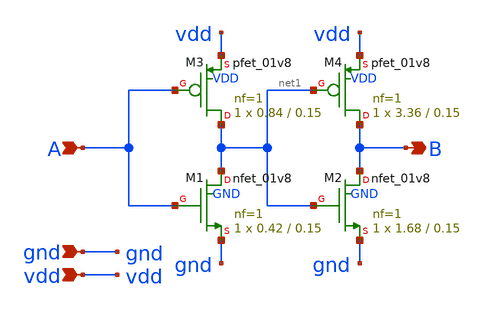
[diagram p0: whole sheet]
** sch_path: xschem/buffer_fo4.sch
**.subckt buffer_fo4 A B vdd gnd
*.ipin A
*.opin B
*.ipin vdd
*.ipin gnd
XM1 net1 A gnd GND sky130_fd_pr__nfet_01v8 L=0.15 W=0.42 nf=1 ad='int((nf+1)/2) * W/nf * 0.29' as='int((nf+2)/2) * W/nf * 0.29'
+ pd='2*int((nf+1)/2) * (W/nf + 0.29)' ps='2*int((nf+2)/2) * (W/nf + 0.29)' nrd='0.29 / W' nrs='0.29 / W'
+ sa=0 sb=0 sd=0 mult=1 m=1
XM2 B net1 gnd GND sky130_fd_pr__nfet_01v8 L=0.15 W=1.68 nf=1 ad='int((nf+1)/2) * W/nf * 0.29' as='int((nf+2)/2) * W/nf * 0.29'
+ pd='2*int((nf+1)/2) * (W/nf + 0.29)' ps='2*int((nf+2)/2) * (W/nf + 0.29)' nrd='0.29 / W' nrs='0.29 / W'
+ sa=0 sb=0 sd=0 mult=1 m=1
XM3 net1 A vdd VDD sky130_fd_pr__pfet_01v8 L=0.15 W=0.84 nf=1 ad='int((nf+1)/2) * W/nf * 0.29' as='int((nf+2)/2) * W/nf * 0.29'
+ pd='2*int((nf+1)/2) * (W/nf + 0.29)' ps='2*int((nf+2)/2) * (W/nf + 0.29)' nrd='0.29 / W' nrs='0.29 / W'
+ sa=0 sb=0 sd=0 mult=1 m=1
XM4 B net1 vdd VDD sky130_fd_pr__pfet_01v8 L=0.15 W=3.36 nf=1 ad='int((nf+1)/2) * W/nf * 0.29' as='int((nf+2)/2) * W/nf * 0.29'
+ pd='2*int((nf+1)/2) * (W/nf + 0.29)' ps='2*int((nf+2)/2) * (W/nf + 0.29)' nrd='0.29 / W' nrs='0.29 / W'
+ sa=0 sb=0 sd=0 mult=1 m=1
**.ends
.end
